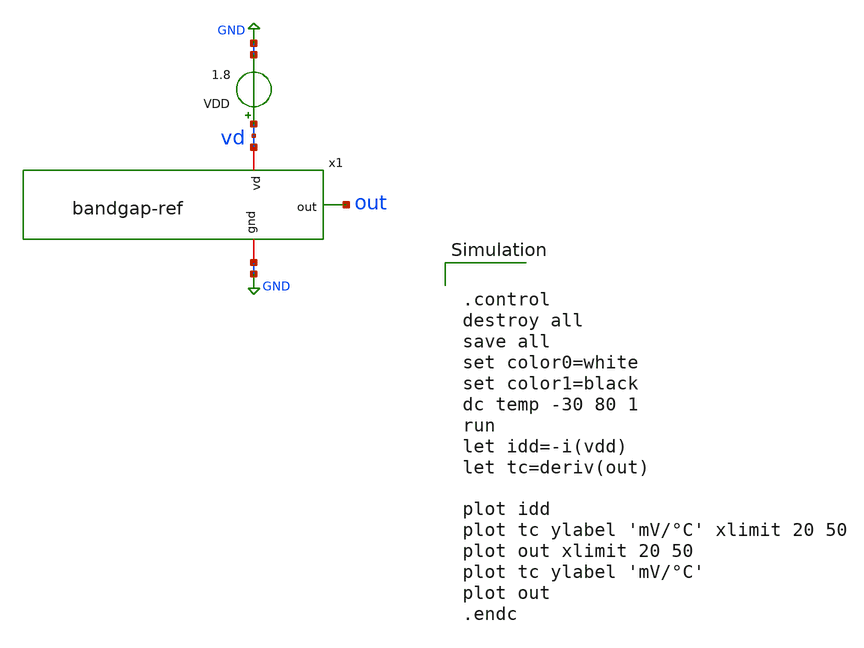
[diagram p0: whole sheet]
** sch_path: bandgap-ref/xschem/bandgap-ref_tb-temp.sch
**.subckt bandgap-ref_tb-temp
VDD vd GND 1.8
x1 vd out GND bandgap-ref
**** begin user architecture code


.control
destroy all
save all
set color0=white
set color1=black
dc temp -30 80 1
run
let idd=-i(vdd)
let tc=deriv(out)

plot idd
plot tc ylabel 'mV/°C' xlimit 20 50
plot out xlimit 20 50
plot tc ylabel 'mV/°C'
plot out
.endc


 .lib $::SKYWATER_MODELS/sky130.lib.spice tt
.include $::SKYWATER_STDCELLS/sky130_fd_sc_hd.spice

**** end user architecture code
**.ends

* expanding   symbol:  /home/hugodg/projects-sky130/temp-sensor/bandgap-ref/xschem/bandgap-ref.sym #
*+ of pins=3
** sym_path: bandgap-ref/xschem/bandgap-ref.sym
** sch_path: bandgap-ref/xschem/bandgap-ref.sch
.subckt bandgap-ref vd out gnd
*.iopin vd
*.iopin gnd
*.opin out
XMN1 net3 net3 gnd gnd sky130_fd_pr__nfet_01v8 L=0.7 W=10 nf=1 ad='int((nf+1)/2) * W/nf * 0.29' as='int((nf+2)/2) * W/nf * 0.29'
+ pd='2*int((nf+1)/2) * (W/nf + 0.29)' ps='2*int((nf+2)/2) * (W/nf + 0.29)' nrd='0.29 / W' nrs='0.29 / W'
+ sa=0 sb=0 sd=0 mult=1 m=1
XMP1 net3 net1 vd vd sky130_fd_pr__pfet_01v8 L=0.7 W=0.83 nf=1 ad='int((nf+1)/2) * W/nf * 0.29' as='int((nf+2)/2) * W/nf * 0.29'
+ pd='2*int((nf+1)/2) * (W/nf + 0.29)' ps='2*int((nf+2)/2) * (W/nf + 0.29)' nrd='0.29 / W' nrs='0.29 / W'
+ sa=0 sb=0 sd=0 mult=1 m=1
XMP2 net1 net1 vd vd sky130_fd_pr__pfet_01v8 L=0.7 W=0.83 nf=1 ad='int((nf+1)/2) * W/nf * 0.29' as='int((nf+2)/2) * W/nf * 0.29'
+ pd='2*int((nf+1)/2) * (W/nf + 0.29)' ps='2*int((nf+2)/2) * (W/nf + 0.29)' nrd='0.29 / W' nrs='0.29 / W'
+ sa=0 sb=0 sd=0 mult=1 m=1
XMP3 out net1 vd vd sky130_fd_pr__pfet_01v8 L=0.7 W=0.83 nf=1 ad='int((nf+1)/2) * W/nf * 0.29' as='int((nf+2)/2) * W/nf * 0.29'
+ pd='2*int((nf+1)/2) * (W/nf + 0.29)' ps='2*int((nf+2)/2) * (W/nf + 0.29)' nrd='0.29 / W' nrs='0.29 / W'
+ sa=0 sb=0 sd=0 mult=1 m=1
XMN2 net1 net3 net2 gnd sky130_fd_pr__nfet_01v8 L=0.7 W=14.5 nf=1 ad='int((nf+1)/2) * W/nf * 0.29' as='int((nf+2)/2) * W/nf * 0.29'
+ pd='2*int((nf+1)/2) * (W/nf + 0.29)' ps='2*int((nf+2)/2) * (W/nf + 0.29)' nrd='0.29 / W' nrs='0.29 / W'
+ sa=0 sb=0 sd=0 mult=1 m=1
XMN3 out out gnd gnd sky130_fd_pr__nfet_01v8 L=8.33 W=0.5 nf=1 ad='int((nf+1)/2) * W/nf * 0.29' as='int((nf+2)/2) * W/nf * 0.29'
+ pd='2*int((nf+1)/2) * (W/nf + 0.29)' ps='2*int((nf+2)/2) * (W/nf + 0.29)' nrd='0.29 / W' nrs='0.29 / W'
+ sa=0 sb=0 sd=0 mult=1 m=1
XMN4 net2 out gnd gnd sky130_fd_pr__nfet_01v8 L=1.7 W=0.5 nf=1 ad='int((nf+1)/2) * W/nf * 0.29' as='int((nf+2)/2) * W/nf * 0.29'
+ pd='2*int((nf+1)/2) * (W/nf + 0.29)' ps='2*int((nf+2)/2) * (W/nf + 0.29)' nrd='0.29 / W' nrs='0.29 / W'
+ sa=0 sb=0 sd=0 mult=1 m=1
XMS2 vd net5 net3 gnd sky130_fd_pr__nfet_01v8 L=0.5 W=5 nf=1 ad='int((nf+1)/2) * W/nf * 0.29' as='int((nf+2)/2) * W/nf * 0.29'
+ pd='2*int((nf+1)/2) * (W/nf + 0.29)' ps='2*int((nf+2)/2) * (W/nf + 0.29)' nrd='0.29 / W' nrs='0.29 / W'
+ sa=0 sb=0 sd=0 mult=1 m=1
XMS1 net1 net4 gnd gnd sky130_fd_pr__nfet_01v8 L=0.5 W=6 nf=1 ad='int((nf+1)/2) * W/nf * 0.29' as='int((nf+2)/2) * W/nf * 0.29'
+ pd='2*int((nf+1)/2) * (W/nf + 0.29)' ps='2*int((nf+2)/2) * (W/nf + 0.29)' nrd='0.29 / W' nrs='0.29 / W'
+ sa=0 sb=0 sd=0 mult=1 m=1
XMD3 net4 net4 vd vd sky130_fd_pr__pfet_01v8 L=0.5 W=0.5 nf=1 ad='int((nf+1)/2) * W/nf * 0.29' as='int((nf+2)/2) * W/nf * 0.29'
+ pd='2*int((nf+1)/2) * (W/nf + 0.29)' ps='2*int((nf+2)/2) * (W/nf + 0.29)' nrd='0.29 / W' nrs='0.29 / W'
+ sa=0 sb=0 sd=0 mult=1 m=1
XMD2 net5 net5 net4 net4 sky130_fd_pr__pfet_01v8 L=0.5 W=0.5 nf=1 ad='int((nf+1)/2) * W/nf * 0.29' as='int((nf+2)/2) * W/nf * 0.29'
+ pd='2*int((nf+1)/2) * (W/nf + 0.29)' ps='2*int((nf+2)/2) * (W/nf + 0.29)' nrd='0.29 / W' nrs='0.29 / W'
+ sa=0 sb=0 sd=0 mult=1 m=1
XMD1 net5 net5 gnd gnd sky130_fd_pr__nfet_01v8 L=0.5 W=0.5 nf=1 ad='int((nf+1)/2) * W/nf * 0.29' as='int((nf+2)/2) * W/nf * 0.29'
+ pd='2*int((nf+1)/2) * (W/nf + 0.29)' ps='2*int((nf+2)/2) * (W/nf + 0.29)' nrd='0.29 / W' nrs='0.29 / W'
+ sa=0 sb=0 sd=0 mult=1 m=1
.ends

.GLOBAL GND
.end
